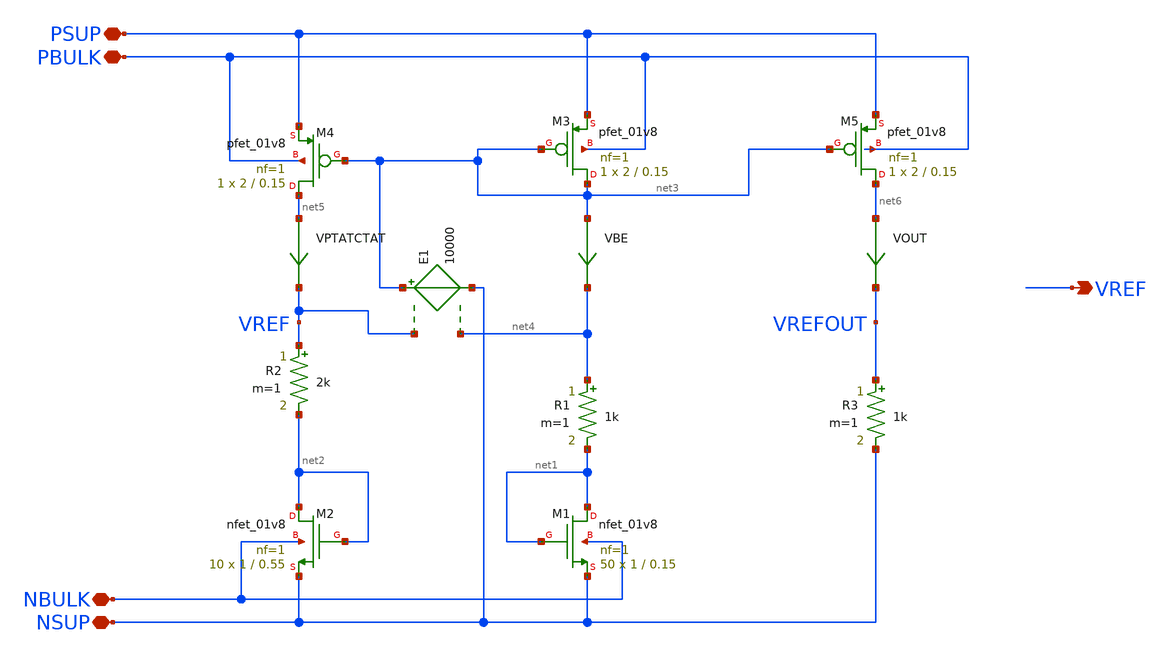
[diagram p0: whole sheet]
** sch_path: xschem/Bandgap.sch
**.subckt Bandgap PSUP NSUP NBULK VREF PBULK
*.iopin PSUP
*.iopin NSUP
*.iopin NBULK
*.opin VREF
*.iopin PBULK
XM1 net1 net1 NSUP NBULK sky130_fd_pr__nfet_01v8 L=0.15 W=1 nf=1 ad='int((1 + 1)/2) * 1 / 1 * 0.29' as='int((1 + 2)/2) * 1 / 1 * 0.29'
+ pd='2*int((1 + 1)/2) * (1 / 1 + 0.29)' ps='2*int((1 + 2)/2) * (1 / 1 + 0.29)' nrd='0.29 / 1 ' nrs='0.29 / 1 '
+ sa=0 sb=0 sd=0 mult=50 m=50
XM2 net2 net2 NSUP NBULK sky130_fd_pr__nfet_01v8 L=0.55 W=1 nf=1 ad='int((1 + 1)/2) * 1 / 1 * 0.29' as='int((1 + 2)/2) * 1 / 1 * 0.29'
+ pd='2*int((1 + 1)/2) * (1 / 1 + 0.29)' ps='2*int((1 + 2)/2) * (1 / 1 + 0.29)' nrd='0.29 / 1 ' nrs='0.29 / 1 '
+ sa=0 sb=0 sd=0 mult=10 m=10
R1 net4 net1 1k m=1
R2 VREF net2 2k m=1
XM3 net3 net3 PSUP PBULK sky130_fd_pr__pfet_01v8 L=0.15 W=2 nf=1 ad='int((nf+1)/2) * W/nf * 0.29' as='int((nf+2)/2) * W/nf * 0.29'
+ pd='2*int((nf+1)/2) * (W/nf + 0.29)' ps='2*int((nf+2)/2) * (W/nf + 0.29)' nrd='0.29 / W' nrs='0.29 / W'
+ sa=0 sb=0 sd=0 mult=1 m=1
XM4 net5 net3 PSUP PBULK sky130_fd_pr__pfet_01v8 L=0.15 W=2 nf=1 ad='int((nf+1)/2) * W/nf * 0.29' as='int((nf+2)/2) * W/nf * 0.29'
+ pd='2*int((nf+1)/2) * (W/nf + 0.29)' ps='2*int((nf+2)/2) * (W/nf + 0.29)' nrd='0.29 / W' nrs='0.29 / W'
+ sa=0 sb=0 sd=0 mult=1 m=1
E1 net3 NSUP VREF net4 10000
VBE net3 net4 0
.save i(vbe)
VPTATCTAT net5 VREF 0
.save i(vptatctat)
XM5 net6 net3 PSUP PBULK sky130_fd_pr__pfet_01v8 L=0.15 W=2 nf=1 ad='int((nf+1)/2) * W/nf * 0.29' as='int((nf+2)/2) * W/nf * 0.29'
+ pd='2*int((nf+1)/2) * (W/nf + 0.29)' ps='2*int((nf+2)/2) * (W/nf + 0.29)' nrd='0.29 / W' nrs='0.29 / W'
+ sa=0 sb=0 sd=0 mult=1 m=1
R3 VREFOUT NSUP 1k m=1
VOUT net6 VREFOUT 0
.save i(vout)
**.ends
.end
